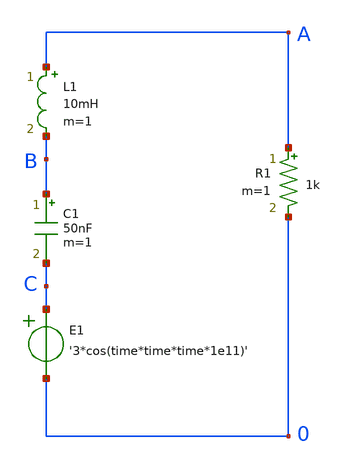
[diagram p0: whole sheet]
** sch_path: rlc.sch
**.subckt rlc
C1 B C 50nF m=1
L1 A B 10mH m=1
R1 A 0 1k m=1
E1 C 0 VOL=' '3*cos(time*time*time*1e11)' '
**** begin user architecture code


.tran 10n 2000u uic
.save all


**** end user architecture code
**.ends
.end
